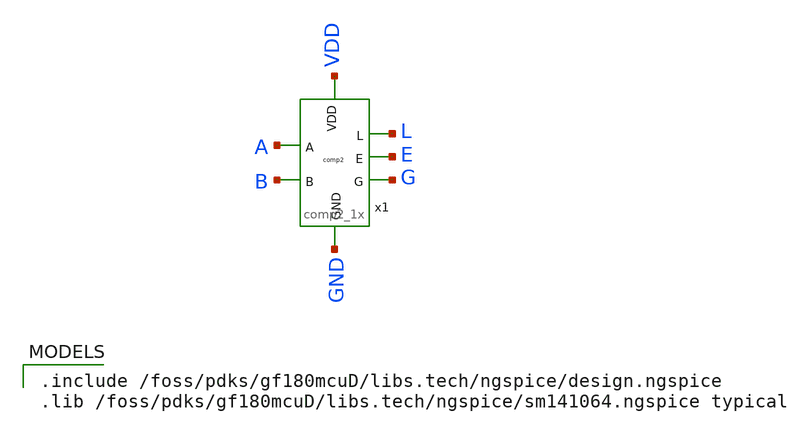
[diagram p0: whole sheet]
** sch_path: cell/comp2/xschem/tb_comp2_1x.sch
**.subckt tb_comp2_1x
x1 VDD L A E G B GND comp2_1x
**** begin user architecture code

.include /foss/pdks/gf180mcuD/libs.tech/ngspice/design.ngspice
.lib /foss/pdks/gf180mcuD/libs.tech/ngspice/sm141064.ngspice typical


* Stimuli
* VPOWER VDD gnd DC 3.3
* V_A A gnd PWL(0 0 {10n-10p} 0 {10n+10p} 3.3 {20n-10p} 3.3 {20n+10p} 0 {30n-10p} 0 {30n+10p} 3.3 40n
*+ 3.3)
* V_B B gnd PWL(0 0 {20n-10p} 0 {20n+10p} 3.3 40n 3.3)

* Simulation
* .tran 1p 40n
* .control
* run
* save all
* plot G E+4 L+8 B+12 A+16
* .endc
* .GLOBAL gnd
* .end


* Define parameters
.GLOBAL gnd
.temp 25
.param vdd = 3.3V
.param slew_in = 10p
.param cload = 1f
.param vh = {vdd/2}
.param v_10 = {vdd*0.1}
.param v_90 = {vdd*0.9}
* For printing purposes
.csparam outload = {1*cload}
.csparam slewin = {1*slew_in}

* Stimuli
VVDD VDD gnd DC {vdd}
V_A A gnd PULSE(0 {vdd} 2n {slew_in} {slew_in} 4n 8n)
V_B B gnd PULSE(0 {vdd} 1n {slew_in} {slew_in} 2n 4n)
* V_A A gnd PWL(0 0 {10n-10p} 0 {10n+10p} 3.3 {20n-10p} 3.3 {20n+10p} 0 {30n-10p} 0 {30n+10p} 3.3 40n
*+ 3.3)
* V_B B gnd PWL(0 0 {20n-10p} 0 {20n+10p} 3.3 40n 3.3)

* Load capacitance
CLL L gnd {cload}
CLE E gnd {cload}
CLG G gnd {cload}

********************************************************************************
* Analysis Statements
********************************************************************************
.OPTIONS SAVE CURRENTS
.tran 1p 10n

* --- Delay and Slew Measurements ---
* These .measure statements are now valid because vh, v_10, and v_90 are defined globally above.

* G (A > B) output
.meas tran g_delay_rise TRIG v(B) VAL=vh FALL=1 TARG v(G) VAL=vh RISE=1
.meas tran g_slew_rise  TRIG v(G) VAL=v_10 RISE=1 TARG v(G) VAL=v_90 RISE=1
.meas tran g_delay_fall TRIG v(B) VAL=vh RISE=1 TARG v(G) VAL=vh FALL=1
.meas tran g_slew_fall  TRIG v(G) VAL=v_90 RISE=1 TARG v(G) VAL=v_10 FALL=1

* L (A < B) output
.meas tran l_delay_rise TRIG v(B) VAL=vh RISE=1 TARG v(L) VAL=vh RISE=1
.meas tran l_slew_rise  TRIG v(L) VAL=v_10 RISE=1 TARG v(L) VAL=v_90 RISE=1
.meas tran l_delay_fall TRIG v(A) VAL=vh RISE=1 TARG v(L) VAL=vh FALL=1
.meas tran l_slew_fall  TRIG v(L) VAL=v_90 FALL=1 TARG v(L) VAL=v_10 FALL=1

* E (A = B) output
.meas tran e_delay_rise_a TRIG v(A) VAL=vh RISE=1 TARG v(E) VAL=vh RISE=1
.meas tran e_slew_rise_a  TRIG v(E) VAL=v_10 RISE=1 TARG v(E) VAL=v_90 RISE=1
.meas tran e_delay_fall_b TRIG v(B) VAL=vh FALL=1 TARG v(E) VAL=vh FALL=1
.meas tran e_slew_fall_b  TRIG v(E) VAL=v_90 FALL=1 TARG v(E) VAL=v_10 FALL=1

* --- Power and Energy Measurements ---
.meas tran avg_current AVG i(vvdd) FROM=0ns TO=8ns
.meas tran i_leak_00 find i(vvdd) at=0.5n
.meas tran i_leak_01 find i(vvdd) at=1.5n
.meas tran i_leak_11 find i(vvdd) at=2.5n
.meas tran i_leak_10 find i(vvdd) at=3.5n

********************************************************************************
* Simulation Control Block
********************************************************************************
.control
	run

	* Delay and Output Transition Time Analysis
	echo "========================================================================"
    	echo "1. Delay and Output Transition Time Analysis"
	echo -n "   Input Slew = "
	echo $&slewin
	echo -n "   Output Load = "
	echo $&outload
    	echo "------------------------------------------------------------------------"
    	print g_delay_rise g_slew_rise g_delay_fall g_slew_fall
    	print l_delay_rise l_slew_rise l_delay_fall l_slew_fall
    	print e_delay_rise_a e_slew_rise_a e_delay_fall_b e_slew_fall_b
.endc
.end

**** end user architecture code
**.ends

* expanding   symbol:  comp2_1x.sym # of pins=7
** sym_path: cell/comp2/xschem/comp2_1x.sym
** sch_path: cell/comp2/xschem/comp2_1x.sch
.subckt comp2_1x VDD L A E G B GND
*.opin L
*.opin G
*.opin E
*.ipin A
*.ipin B
*.ipin VDD
*.ipin GND
XM17 net1 NOT_A VDD VDD pfet_03v3 L=0.3u W=1.7u nf=1 ad='int((nf+1)/2) * W/nf * 0.18u' as='int((nf+2)/2) * W/nf * 0.18u'
+ pd='2*int((nf+1)/2) * (W/nf + 0.18u)' ps='2*int((nf+2)/2) * (W/nf + 0.18u)' nrd='0.18u / W' nrs='0.18u / W'
+ sa=0 sb=0 sd=0 m=1
XM18 E A net1 VDD pfet_03v3 L=0.3u W=1.7u nf=1 ad='int((nf+1)/2) * W/nf * 0.18u' as='int((nf+2)/2) * W/nf * 0.18u'
+ pd='2*int((nf+1)/2) * (W/nf + 0.18u)' ps='2*int((nf+2)/2) * (W/nf + 0.18u)' nrd='0.18u / W' nrs='0.18u / W'
+ sa=0 sb=0 sd=0 m=1
XM19 net1 B VDD VDD pfet_03v3 L=0.3u W=1.7u nf=1 ad='int((nf+1)/2) * W/nf * 0.18u' as='int((nf+2)/2) * W/nf * 0.18u'
+ pd='2*int((nf+1)/2) * (W/nf + 0.18u)' ps='2*int((nf+2)/2) * (W/nf + 0.18u)' nrd='0.18u / W' nrs='0.18u / W'
+ sa=0 sb=0 sd=0 m=1
XM20 E NOT_B net1 VDD pfet_03v3 L=0.3u W=1.7u nf=1 ad='int((nf+1)/2) * W/nf * 0.18u' as='int((nf+2)/2) * W/nf * 0.18u'
+ pd='2*int((nf+1)/2) * (W/nf + 0.18u)' ps='2*int((nf+2)/2) * (W/nf + 0.18u)' nrd='0.18u / W' nrs='0.18u / W'
+ sa=0 sb=0 sd=0 m=1
XM21 E NOT_A net2 GND nfet_03v3 L=0.3u W=0.85u nf=1 ad='int((nf+1)/2) * W/nf * 0.18u' as='int((nf+2)/2) * W/nf * 0.18u'
+ pd='2*int((nf+1)/2) * (W/nf + 0.18u)' ps='2*int((nf+2)/2) * (W/nf + 0.18u)' nrd='0.18u / W' nrs='0.18u / W'
+ sa=0 sb=0 sd=0 m=1
XM22 net2 B GND GND nfet_03v3 L=0.3u W=0.85u nf=1 ad='int((nf+1)/2) * W/nf * 0.18u' as='int((nf+2)/2) * W/nf * 0.18u'
+ pd='2*int((nf+1)/2) * (W/nf + 0.18u)' ps='2*int((nf+2)/2) * (W/nf + 0.18u)' nrd='0.18u / W' nrs='0.18u / W'
+ sa=0 sb=0 sd=0 m=1
XM23 E A net3 GND nfet_03v3 L=0.3u W=0.85u nf=1 ad='int((nf+1)/2) * W/nf * 0.18u' as='int((nf+2)/2) * W/nf * 0.18u'
+ pd='2*int((nf+1)/2) * (W/nf + 0.18u)' ps='2*int((nf+2)/2) * (W/nf + 0.18u)' nrd='0.18u / W' nrs='0.18u / W'
+ sa=0 sb=0 sd=0 m=1
XM24 net3 NOT_B GND GND nfet_03v3 L=0.3u W=0.85u nf=1 ad='int((nf+1)/2) * W/nf * 0.18u' as='int((nf+2)/2) * W/nf * 0.18u'
+ pd='2*int((nf+1)/2) * (W/nf + 0.18u)' ps='2*int((nf+2)/2) * (W/nf + 0.18u)' nrd='0.18u / W' nrs='0.18u / W'
+ sa=0 sb=0 sd=0 m=1
XM1 NOT_B B GND GND nfet_03v3 L=0.3u W=0.85u nf=1 ad='int((nf+1)/2) * W/nf * 0.18u' as='int((nf+2)/2) * W/nf * 0.18u'
+ pd='2*int((nf+1)/2) * (W/nf + 0.18u)' ps='2*int((nf+2)/2) * (W/nf + 0.18u)' nrd='0.18u / W' nrs='0.18u / W'
+ sa=0 sb=0 sd=0 m=1
XM2 NOT_B B VDD VDD pfet_03v3 L=0.3u W=1.7u nf=1 ad='int((nf+1)/2) * W/nf * 0.18u' as='int((nf+2)/2) * W/nf * 0.18u'
+ pd='2*int((nf+1)/2) * (W/nf + 0.18u)' ps='2*int((nf+2)/2) * (W/nf + 0.18u)' nrd='0.18u / W' nrs='0.18u / W'
+ sa=0 sb=0 sd=0 m=1
XM3 NOT_A A GND GND nfet_03v3 L=0.3u W=0.85u nf=1 ad='int((nf+1)/2) * W/nf * 0.18u' as='int((nf+2)/2) * W/nf * 0.18u'
+ pd='2*int((nf+1)/2) * (W/nf + 0.18u)' ps='2*int((nf+2)/2) * (W/nf + 0.18u)' nrd='0.18u / W' nrs='0.18u / W'
+ sa=0 sb=0 sd=0 m=1
XM4 NOT_A A VDD VDD pfet_03v3 L=0.3u W=1.7u nf=1 ad='int((nf+1)/2) * W/nf * 0.18u' as='int((nf+2)/2) * W/nf * 0.18u'
+ pd='2*int((nf+1)/2) * (W/nf + 0.18u)' ps='2*int((nf+2)/2) * (W/nf + 0.18u)' nrd='0.18u / W' nrs='0.18u / W'
+ sa=0 sb=0 sd=0 m=1
XM5 net5 NOT_A net4 GND nfet_03v3 L=0.3u W=0.85u nf=1 ad='int((nf+1)/2) * W/nf * 0.18u' as='int((nf+2)/2) * W/nf * 0.18u'
+ pd='2*int((nf+1)/2) * (W/nf + 0.18u)' ps='2*int((nf+2)/2) * (W/nf + 0.18u)' nrd='0.18u / W' nrs='0.18u / W'
+ sa=0 sb=0 sd=0 m=1
XM6 net4 B GND GND nfet_03v3 L=0.3u W=0.85u nf=1 ad='int((nf+1)/2) * W/nf * 0.18u' as='int((nf+2)/2) * W/nf * 0.18u'
+ pd='2*int((nf+1)/2) * (W/nf + 0.18u)' ps='2*int((nf+2)/2) * (W/nf + 0.18u)' nrd='0.18u / W' nrs='0.18u / W'
+ sa=0 sb=0 sd=0 m=1
XM7 net5 B VDD VDD pfet_03v3 L=0.3u W=1.7u nf=1 ad='int((nf+1)/2) * W/nf * 0.18u' as='int((nf+2)/2) * W/nf * 0.18u'
+ pd='2*int((nf+1)/2) * (W/nf + 0.18u)' ps='2*int((nf+2)/2) * (W/nf + 0.18u)' nrd='0.18u / W' nrs='0.18u / W'
+ sa=0 sb=0 sd=0 m=1
XM8 net5 NOT_A VDD VDD pfet_03v3 L=0.3u W=1.7u nf=1 ad='int((nf+1)/2) * W/nf * 0.18u' as='int((nf+2)/2) * W/nf * 0.18u'
+ pd='2*int((nf+1)/2) * (W/nf + 0.18u)' ps='2*int((nf+2)/2) * (W/nf + 0.18u)' nrd='0.18u / W' nrs='0.18u / W'
+ sa=0 sb=0 sd=0 m=1
XM9 L net5 GND GND nfet_03v3 L=0.3u W=0.85u nf=1 ad='int((nf+1)/2) * W/nf * 0.18u' as='int((nf+2)/2) * W/nf * 0.18u'
+ pd='2*int((nf+1)/2) * (W/nf + 0.18u)' ps='2*int((nf+2)/2) * (W/nf + 0.18u)' nrd='0.18u / W' nrs='0.18u / W'
+ sa=0 sb=0 sd=0 m=1
XM10 L net5 VDD VDD pfet_03v3 L=0.3u W=1.7u nf=1 ad='int((nf+1)/2) * W/nf * 0.18u' as='int((nf+2)/2) * W/nf * 0.18u'
+ pd='2*int((nf+1)/2) * (W/nf + 0.18u)' ps='2*int((nf+2)/2) * (W/nf + 0.18u)' nrd='0.18u / W' nrs='0.18u / W'
+ sa=0 sb=0 sd=0 m=1
XM11 net7 A net6 GND nfet_03v3 L=0.3u W=0.85u nf=1 ad='int((nf+1)/2) * W/nf * 0.18u' as='int((nf+2)/2) * W/nf * 0.18u'
+ pd='2*int((nf+1)/2) * (W/nf + 0.18u)' ps='2*int((nf+2)/2) * (W/nf + 0.18u)' nrd='0.18u / W' nrs='0.18u / W'
+ sa=0 sb=0 sd=0 m=1
XM12 net6 NOT_B GND GND nfet_03v3 L=0.3u W=0.85u nf=1 ad='int((nf+1)/2) * W/nf * 0.18u' as='int((nf+2)/2) * W/nf * 0.18u'
+ pd='2*int((nf+1)/2) * (W/nf + 0.18u)' ps='2*int((nf+2)/2) * (W/nf + 0.18u)' nrd='0.18u / W' nrs='0.18u / W'
+ sa=0 sb=0 sd=0 m=1
XM13 net7 NOT_B VDD VDD pfet_03v3 L=0.3u W=1.7u nf=1 ad='int((nf+1)/2) * W/nf * 0.18u' as='int((nf+2)/2) * W/nf * 0.18u'
+ pd='2*int((nf+1)/2) * (W/nf + 0.18u)' ps='2*int((nf+2)/2) * (W/nf + 0.18u)' nrd='0.18u / W' nrs='0.18u / W'
+ sa=0 sb=0 sd=0 m=1
XM14 net7 A VDD VDD pfet_03v3 L=0.3u W=1.7u nf=1 ad='int((nf+1)/2) * W/nf * 0.18u' as='int((nf+2)/2) * W/nf * 0.18u'
+ pd='2*int((nf+1)/2) * (W/nf + 0.18u)' ps='2*int((nf+2)/2) * (W/nf + 0.18u)' nrd='0.18u / W' nrs='0.18u / W'
+ sa=0 sb=0 sd=0 m=1
XM15 G net7 GND GND nfet_03v3 L=0.3u W=0.85u nf=1 ad='int((nf+1)/2) * W/nf * 0.18u' as='int((nf+2)/2) * W/nf * 0.18u'
+ pd='2*int((nf+1)/2) * (W/nf + 0.18u)' ps='2*int((nf+2)/2) * (W/nf + 0.18u)' nrd='0.18u / W' nrs='0.18u / W'
+ sa=0 sb=0 sd=0 m=1
XM16 G net7 VDD VDD pfet_03v3 L=0.3u W=1.7u nf=1 ad='int((nf+1)/2) * W/nf * 0.18u' as='int((nf+2)/2) * W/nf * 0.18u'
+ pd='2*int((nf+1)/2) * (W/nf + 0.18u)' ps='2*int((nf+2)/2) * (W/nf + 0.18u)' nrd='0.18u / W' nrs='0.18u / W'
+ sa=0 sb=0 sd=0 m=1
.ends

.end
